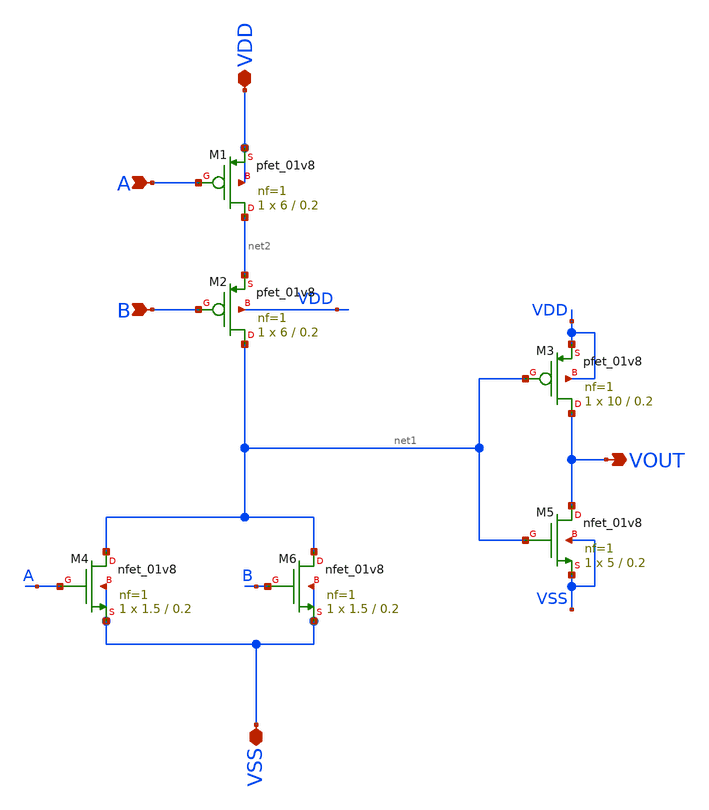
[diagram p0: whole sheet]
** sch_path: Xschem/DIVIDER/OR.sch
**.subckt OR VSS VDD A B VOUT
*.iopin VSS
*.iopin VDD
*.ipin A
*.ipin B
*.opin VOUT
XM1 net2 A VDD VDD sky130_fd_pr__pfet_01v8 L=0.2 W=6 nf=1 ad='int((nf+1)/2) * W/nf * 0.29' as='int((nf+2)/2) * W/nf * 0.29'
+ pd='2*int((nf+1)/2) * (W/nf + 0.29)' ps='2*int((nf+2)/2) * (W/nf + 0.29)' nrd='0.29 / W' nrs='0.29 / W'
+ sa=0 sb=0 sd=0 mult=1 m=1
XM2 net1 B net2 VDD sky130_fd_pr__pfet_01v8 L=0.2 W=6 nf=1 ad='int((nf+1)/2) * W/nf * 0.29' as='int((nf+2)/2) * W/nf * 0.29'
+ pd='2*int((nf+1)/2) * (W/nf + 0.29)' ps='2*int((nf+2)/2) * (W/nf + 0.29)' nrd='0.29 / W' nrs='0.29 / W'
+ sa=0 sb=0 sd=0 mult=1 m=1
XM3 VOUT net1 VDD VDD sky130_fd_pr__pfet_01v8 L=0.2 W=10 nf=1 ad='int((nf+1)/2) * W/nf * 0.29' as='int((nf+2)/2) * W/nf * 0.29'
+ pd='2*int((nf+1)/2) * (W/nf + 0.29)' ps='2*int((nf+2)/2) * (W/nf + 0.29)' nrd='0.29 / W' nrs='0.29 / W'
+ sa=0 sb=0 sd=0 mult=1 m=1
XM4 net1 A VSS VSS sky130_fd_pr__nfet_01v8 L=0.2 W=1.5 nf=1 ad='int((nf+1)/2) * W/nf * 0.29' as='int((nf+2)/2) * W/nf * 0.29'
+ pd='2*int((nf+1)/2) * (W/nf + 0.29)' ps='2*int((nf+2)/2) * (W/nf + 0.29)' nrd='0.29 / W' nrs='0.29 / W'
+ sa=0 sb=0 sd=0 mult=1 m=1
XM5 VOUT net1 VSS VSS sky130_fd_pr__nfet_01v8 L=0.2 W=5 nf=1 ad='int((nf+1)/2) * W/nf * 0.29' as='int((nf+2)/2) * W/nf * 0.29'
+ pd='2*int((nf+1)/2) * (W/nf + 0.29)' ps='2*int((nf+2)/2) * (W/nf + 0.29)' nrd='0.29 / W' nrs='0.29 / W'
+ sa=0 sb=0 sd=0 mult=1 m=1
XM6 net1 B VSS VSS sky130_fd_pr__nfet_01v8 L=0.2 W=1.5 nf=1 ad='int((nf+1)/2) * W/nf * 0.29' as='int((nf+2)/2) * W/nf * 0.29'
+ pd='2*int((nf+1)/2) * (W/nf + 0.29)' ps='2*int((nf+2)/2) * (W/nf + 0.29)' nrd='0.29 / W' nrs='0.29 / W'
+ sa=0 sb=0 sd=0 mult=1 m=1
**.ends
.end
